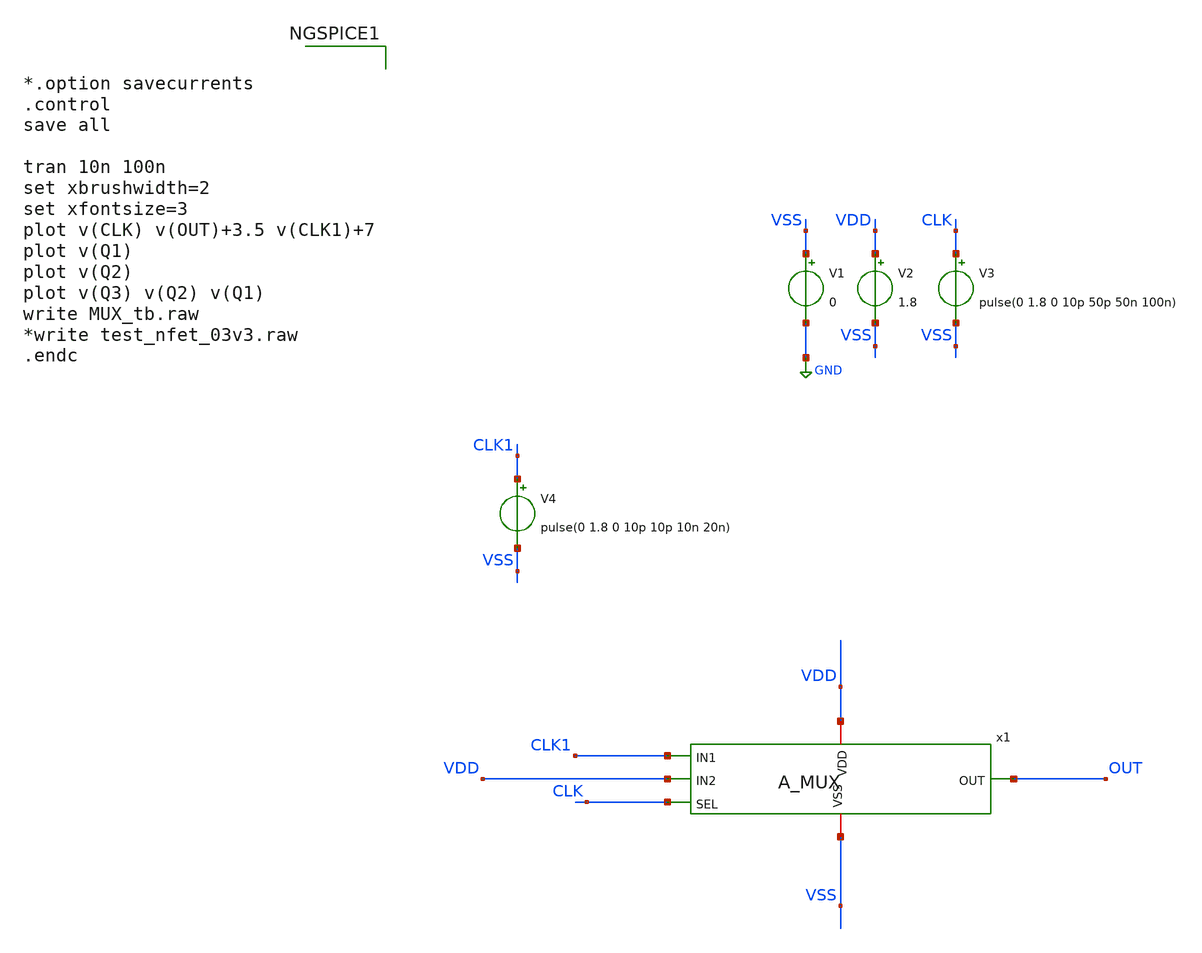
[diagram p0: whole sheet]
** sch_path: Xschem/PLL_TOP_Schematics/MUX_tb.sch
**.subckt MUX_tb
V1 VSS GND 0
V2 VDD VSS 1.8
V3 CLK VSS pulse(0 1.8 0 10p 50p 50n 100n)
x1 VDD VSS CLK1 VDD CLK OUT A_MUX
V4 CLK1 VSS pulse(0 1.8 0 10p 10p 10n 20n)
**** begin user architecture code


*.option savecurrents
.control
save all

tran 10n 100n
set xbrushwidth=2
set xfontsize=3
plot v(CLK) v(OUT)+3.5 v(CLK1)+7
plot v(Q1)
plot v(Q2)
plot v(Q3) v(Q2) v(Q1)
write MUX_tb.raw
*write test_nfet_03v3.raw
.endc



** opencircuitdesign pdks install
.lib $::SKYWATER_MODELS/sky130.lib.spice tt


**** end user architecture code
**.ends
.GLOBAL GND
.end
